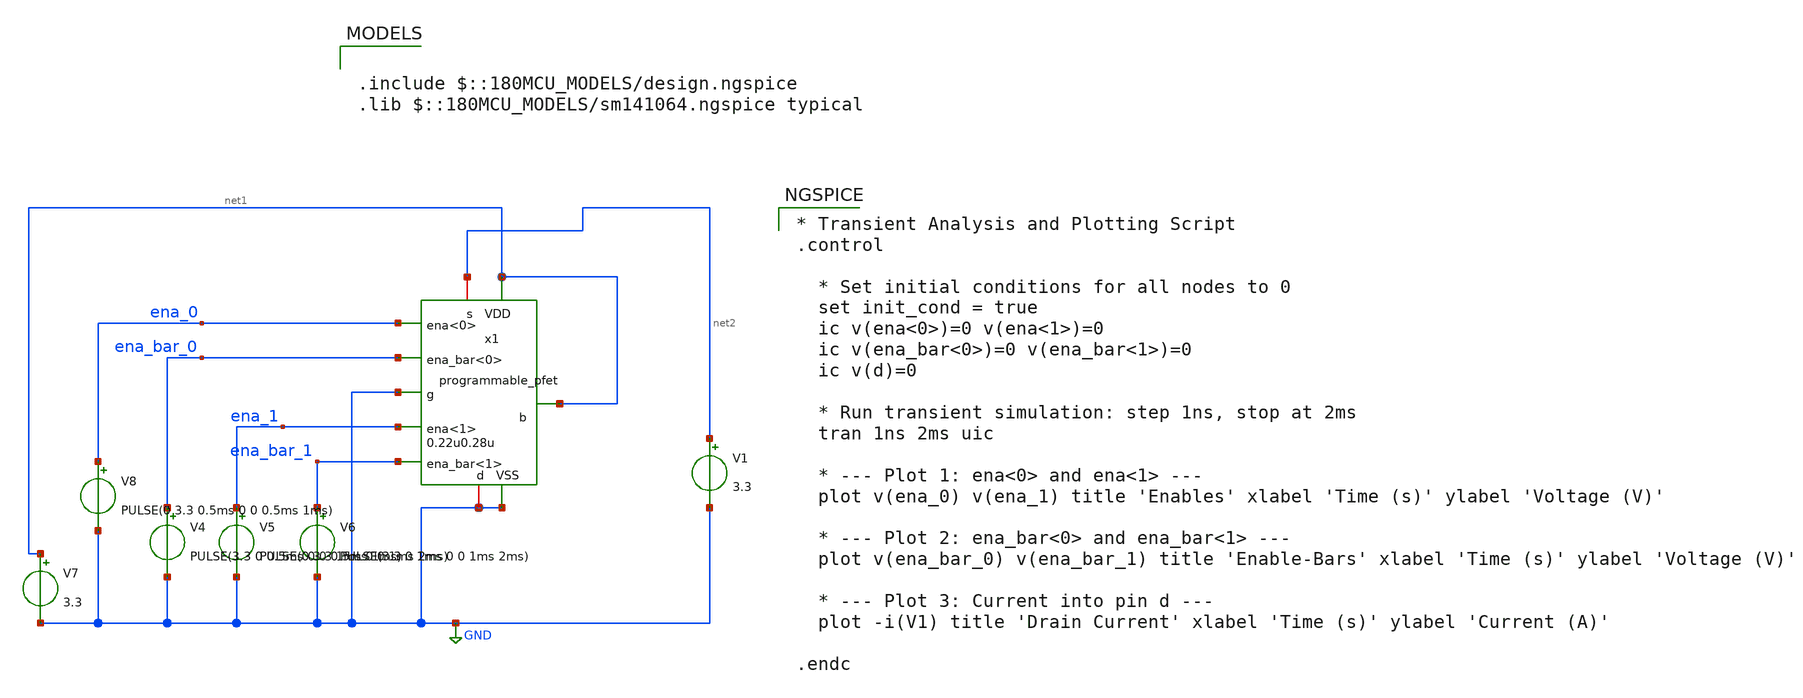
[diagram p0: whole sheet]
** sch_path: designs/libs/core_digital/TB_prog_fet.sch
**.subckt TB_prog_fet
V4 ena_bar_0 GND PULSE(3.3 0 0.5ms 0 0 0.5ms 1ms)
V5 ena_1 GND PULSE(0 3.3 1ms 0 0 1ms 2ms)
V6 ena_bar_1 GND PULSE(3.3 0 1ms 0 0 1ms 2ms)
V7 net1 GND 3.3
V8 ena_0 GND PULSE(0 3.3 0.5ms 0 0 0.5ms 1ms)
V1 net2 GND 3.3
x1 GND net1 GND net2 ena_bar_0 net1 ena_bar_1 ena_0 ena_1 GND programmable_pfet width=0.22u
+ length=0.28u
**** begin user architecture code

.include $::180MCU_MODELS/design.ngspice
.lib $::180MCU_MODELS/sm141064.ngspice typical


* Transient Analysis and Plotting Script
.control

  * Set initial conditions for all nodes to 0
  set init_cond = true
  ic v(ena<0>)=0 v(ena<1>)=0
  ic v(ena_bar<0>)=0 v(ena_bar<1>)=0
  ic v(d)=0

  * Run transient simulation: step 1ns, stop at 2ms
  tran 1ns 2ms uic

  * --- Plot 1: ena<0> and ena<1> ---
  plot v(ena_0) v(ena_1) title 'Enables' xlabel 'Time (s)' ylabel 'Voltage (V)'

  * --- Plot 2: ena_bar<0> and ena_bar<1> ---
  plot v(ena_bar_0) v(ena_bar_1) title 'Enable-Bars' xlabel 'Time (s)' ylabel 'Voltage (V)'

  * --- Plot 3: Current into pin d ---
  plot -i(V1) title 'Drain Current' xlabel 'Time (s)' ylabel 'Current (A)'

.endc

**** end user architecture code
**.ends
.GLOBAL GND
.end
